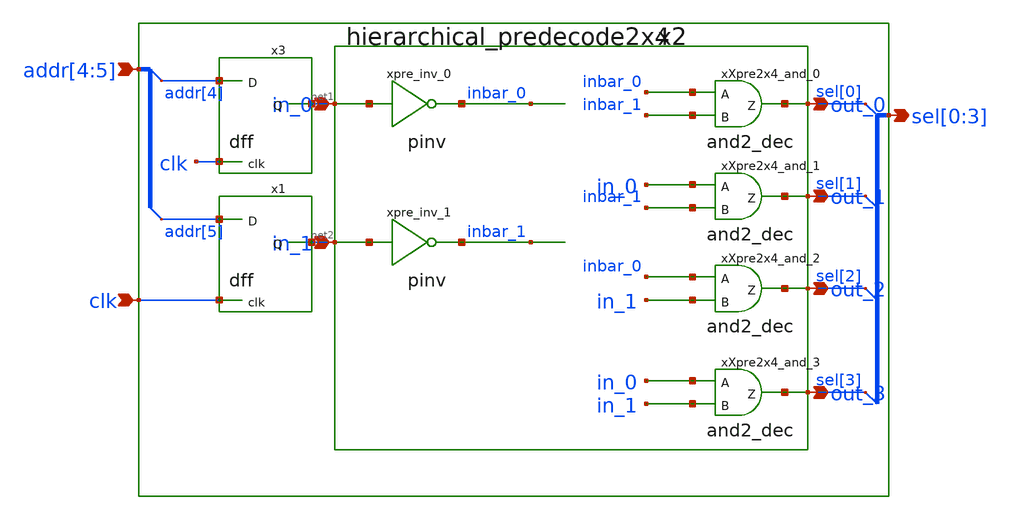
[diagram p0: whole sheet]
** sch_path: sram_2_64_scn4m_lcc/col_decoder.sch
**.subckt col_decoder addr[4],addr[5] clk sel[0],sel[1],sel[2],sel[3]
*.ipin addr[4],addr[5]
*.ipin clk
*.opin sel[0],sel[1],sel[2],sel[3]
x2 net1 net2 sel[0] sel[1] sel[2] sel[3] vdd gnd hierarchical_predecode2x4
x3 addr[4] net1 clk vdd gnd dff
x1 addr[5] net2 clk vdd gnd dff
**.ends
.end
